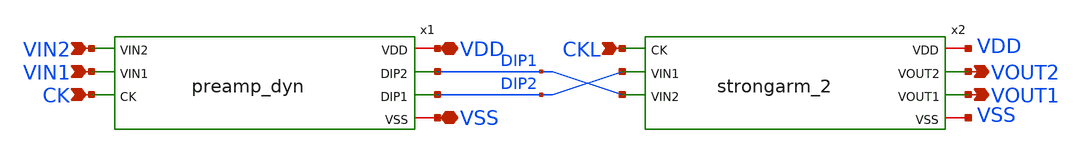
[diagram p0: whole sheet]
** sch_path: comparator_alt/schematic/comparator_2stage.sch
**.subckt comparator_2stage CK VDD VSS VIN1 VIN2 VOUT2 VOUT1 CKL
*.ipin CK
*.iopin VDD
*.iopin VSS
*.ipin VIN1
*.ipin VIN2
*.opin VOUT2
*.opin VOUT1
*.ipin CKL
x1 VDD DIP1 DIP2 VIN2 VIN1 CK VSS preamp_dyn
x2 VDD CKL VOUT2 VOUT1 DIP2 DIP1 VSS strongarm_2
**.ends

* expanding   symbol:  comparator_alt/schematic/preamp_dyn.sym # of pins=7
** sym_path: comparator_alt/schematic/preamp_dyn.sym
** sch_path: comparator_alt/schematic/preamp_dyn.sch
.subckt preamp_dyn VDD DIP2 DIP1 VIN2 VIN1 CK VSS
*.ipin VIN1
*.ipin VIN2
*.iopin VDD
*.iopin VSS
*.opin DIP1
*.opin DIP2
*.ipin CK
XM1P DIP1 VIN1 TAIL VSS nfet_03v3 L=1u W=4u nf=1 ad='int((nf+1)/2) * W/nf * 0.18u' as='int((nf+2)/2) * W/nf * 0.18u'
+ pd='2*int((nf+1)/2) * (W/nf + 0.18u)' ps='2*int((nf+2)/2) * (W/nf + 0.18u)' nrd='0.18u / W' nrs='0.18u / W'
+ sa=0 sb=0 sd=0 m=16
XMT1 TAIL CK VSS VSS nfet_03v3 L=1u W=1u nf=1 ad='int((nf+1)/2) * W/nf * 0.18u' as='int((nf+2)/2) * W/nf * 0.18u'
+ pd='2*int((nf+1)/2) * (W/nf + 0.18u)' ps='2*int((nf+2)/2) * (W/nf + 0.18u)' nrd='0.18u / W' nrs='0.18u / W'
+ sa=0 sb=0 sd=0 m=1
XM2P DIP2 VIN2 TAIL VSS nfet_03v3 L=1u W=4u nf=1 ad='int((nf+1)/2) * W/nf * 0.18u' as='int((nf+2)/2) * W/nf * 0.18u'
+ pd='2*int((nf+1)/2) * (W/nf + 0.18u)' ps='2*int((nf+2)/2) * (W/nf + 0.18u)' nrd='0.18u / W' nrs='0.18u / W'
+ sa=0 sb=0 sd=0 m=16
XMP1 DIP1 CK VDD VDD pfet_03v3 L=0.3u W=3u nf=1 ad='int((nf+1)/2) * W/nf * 0.18u' as='int((nf+2)/2) * W/nf * 0.18u'
+ pd='2*int((nf+1)/2) * (W/nf + 0.18u)' ps='2*int((nf+2)/2) * (W/nf + 0.18u)' nrd='0.18u / W' nrs='0.18u / W'
+ sa=0 sb=0 sd=0 m=1
XMP2 DIP2 CK VDD VDD pfet_03v3 L=0.3u W=3u nf=1 ad='int((nf+1)/2) * W/nf * 0.18u' as='int((nf+2)/2) * W/nf * 0.18u'
+ pd='2*int((nf+1)/2) * (W/nf + 0.18u)' ps='2*int((nf+2)/2) * (W/nf + 0.18u)' nrd='0.18u / W' nrs='0.18u / W'
+ sa=0 sb=0 sd=0 m=1
.ends


* expanding   symbol:  comparator_alt/schematic/strongarm_2.sym # of pins=7
** sym_path: comparator_alt/schematic/strongarm_2.sym
** sch_path: comparator_alt/schematic/strongarm_2.sch
.subckt strongarm_2 VDD CK VOUT2 VOUT1 VIN1 VIN2 VSS
*.opin VOUT1
*.opin VOUT2
*.ipin VIN1
*.ipin VIN2
*.ipin CK
*.iopin VDD
*.iopin VSS
XM1 VOUT2 VOUT1 net1 VSS nfet_03v3 L=0.28u W=2u nf=1 ad='int((nf+1)/2) * W/nf * 0.18u' as='int((nf+2)/2) * W/nf * 0.18u'
+ pd='2*int((nf+1)/2) * (W/nf + 0.18u)' ps='2*int((nf+2)/2) * (W/nf + 0.18u)' nrd='0.18u / W' nrs='0.18u / W'
+ sa=0 sb=0 sd=0 m=1
XM2 VOUT1 VOUT2 VDD VDD pfet_03v3 L=0.28u W=0.42u nf=1 ad='int((nf+1)/2) * W/nf * 0.18u' as='int((nf+2)/2) * W/nf * 0.18u'
+ pd='2*int((nf+1)/2) * (W/nf + 0.18u)' ps='2*int((nf+2)/2) * (W/nf + 0.18u)' nrd='0.18u / W' nrs='0.18u / W'
+ sa=0 sb=0 sd=0 m=1
XM3 VOUT1 CK VDD VDD pfet_03v3 L=0.28u W=5u nf=1 ad='int((nf+1)/2) * W/nf * 0.18u' as='int((nf+2)/2) * W/nf * 0.18u'
+ pd='2*int((nf+1)/2) * (W/nf + 0.18u)' ps='2*int((nf+2)/2) * (W/nf + 0.18u)' nrd='0.18u / W' nrs='0.18u / W'
+ sa=0 sb=0 sd=0 m=1
XM4 net3 CK VDD VDD pfet_03v3 L=0.28u W=5u nf=1 ad='int((nf+1)/2) * W/nf * 0.18u' as='int((nf+2)/2) * W/nf * 0.18u'
+ pd='2*int((nf+1)/2) * (W/nf + 0.18u)' ps='2*int((nf+2)/2) * (W/nf + 0.18u)' nrd='0.18u / W' nrs='0.18u / W'
+ sa=0 sb=0 sd=0 m=1
XM5 net1 CK VDD VDD pfet_03v3 L=0.28u W=5u nf=1 ad='int((nf+1)/2) * W/nf * 0.18u' as='int((nf+2)/2) * W/nf * 0.18u'
+ pd='2*int((nf+1)/2) * (W/nf + 0.18u)' ps='2*int((nf+2)/2) * (W/nf + 0.18u)' nrd='0.18u / W' nrs='0.18u / W'
+ sa=0 sb=0 sd=0 m=1
XM6 VOUT2 CK VDD VDD pfet_03v3 L=0.28u W=5u nf=1 ad='int((nf+1)/2) * W/nf * 0.18u' as='int((nf+2)/2) * W/nf * 0.18u'
+ pd='2*int((nf+1)/2) * (W/nf + 0.18u)' ps='2*int((nf+2)/2) * (W/nf + 0.18u)' nrd='0.18u / W' nrs='0.18u / W'
+ sa=0 sb=0 sd=0 m=1
XM7 VOUT2 VOUT1 VDD VDD pfet_03v3 L=0.28u W=0.42u nf=1 ad='int((nf+1)/2) * W/nf * 0.18u' as='int((nf+2)/2) * W/nf * 0.18u'
+ pd='2*int((nf+1)/2) * (W/nf + 0.18u)' ps='2*int((nf+2)/2) * (W/nf + 0.18u)' nrd='0.18u / W' nrs='0.18u / W'
+ sa=0 sb=0 sd=0 m=1
XM8 net1 VIN2 net2 VSS nfet_03v3 L=1u W=8u nf=1 ad='int((nf+1)/2) * W/nf * 0.18u' as='int((nf+2)/2) * W/nf * 0.18u'
+ pd='2*int((nf+1)/2) * (W/nf + 0.18u)' ps='2*int((nf+2)/2) * (W/nf + 0.18u)' nrd='0.18u / W' nrs='0.18u / W'
+ sa=0 sb=0 sd=0 m=1
XM9 VOUT1 VOUT2 net3 VSS nfet_03v3 L=0.28u W=2u nf=1 ad='int((nf+1)/2) * W/nf * 0.18u' as='int((nf+2)/2) * W/nf * 0.18u'
+ pd='2*int((nf+1)/2) * (W/nf + 0.18u)' ps='2*int((nf+2)/2) * (W/nf + 0.18u)' nrd='0.18u / W' nrs='0.18u / W'
+ sa=0 sb=0 sd=0 m=1
XM10 net3 VIN1 net2 VSS nfet_03v3 L=1u W=8u nf=1 ad='int((nf+1)/2) * W/nf * 0.18u' as='int((nf+2)/2) * W/nf * 0.18u'
+ pd='2*int((nf+1)/2) * (W/nf + 0.18u)' ps='2*int((nf+2)/2) * (W/nf + 0.18u)' nrd='0.18u / W' nrs='0.18u / W'
+ sa=0 sb=0 sd=0 m=1
XM11 net2 CK VSS VSS nfet_03v3 L=0.28u W=2u nf=1 ad='int((nf+1)/2) * W/nf * 0.18u' as='int((nf+2)/2) * W/nf * 0.18u'
+ pd='2*int((nf+1)/2) * (W/nf + 0.18u)' ps='2*int((nf+2)/2) * (W/nf + 0.18u)' nrd='0.18u / W' nrs='0.18u / W'
+ sa=0 sb=0 sd=0 m=1
.ends

.end
